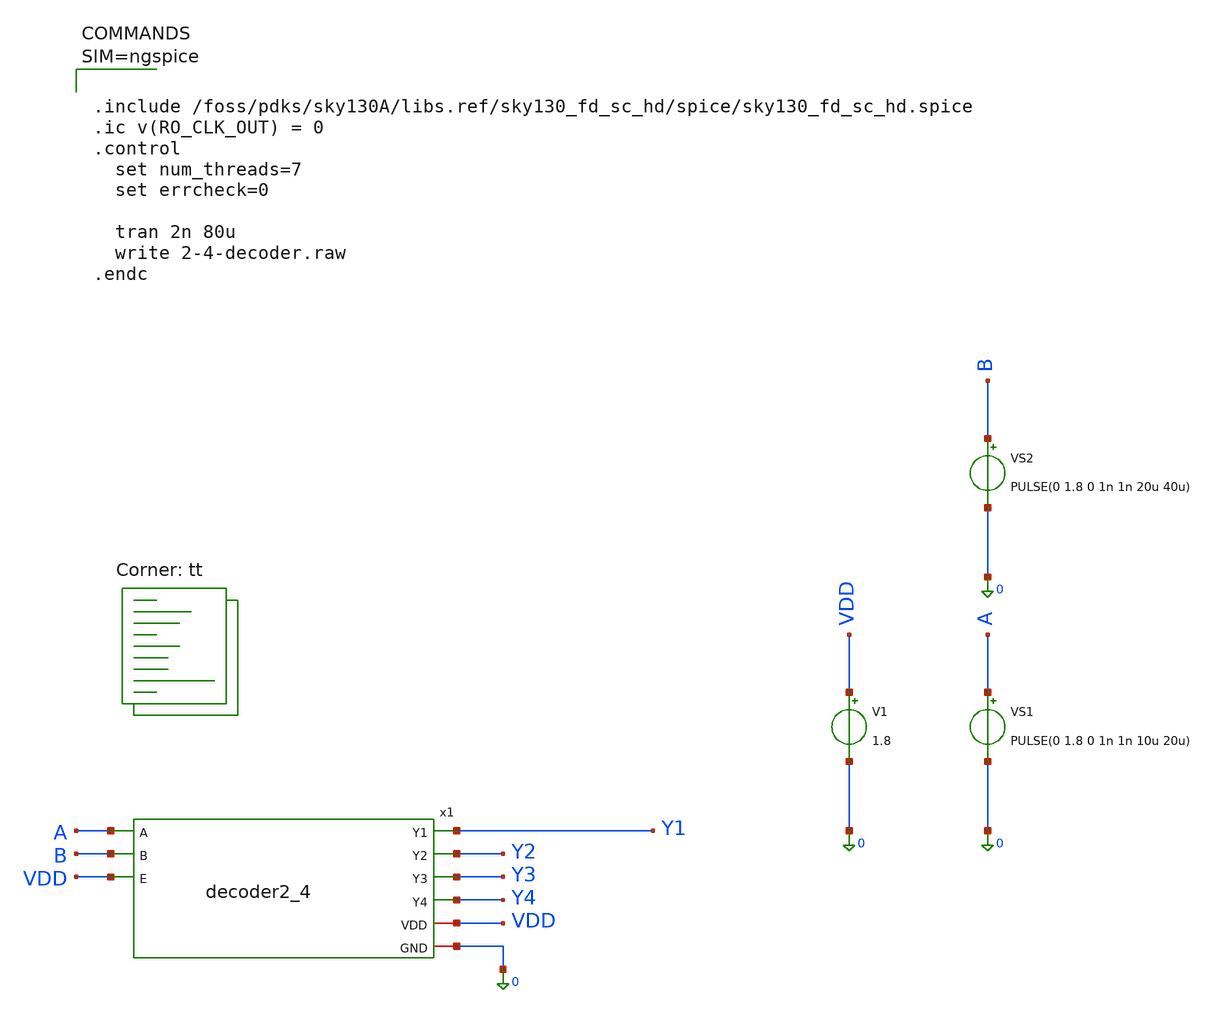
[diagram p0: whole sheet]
** sch_path: src/analog_source_files/decoder2_4_tb.sch
**.subckt decoder2_4_tb
V1 VDD 0 1.8
VS1 A 0 PULSE(0 1.8 0 1n 1n 10u 20u)
VS2 B 0 PULSE(0 1.8 0 1n 1n 20u 40u)
x1 A B Y1 Y2 Y3 Y4 VDD VDD 0 decoder2_4
**** begin user architecture code
.lib $::SKYWATER_MODELS/sky130.lib.spice tt



.include /foss/pdks/sky130A/libs.ref/sky130_fd_sc_hd/spice/sky130_fd_sc_hd.spice
.ic v(RO_CLK_OUT) = 0
.control
  set num_threads=7
  set errcheck=0

  tran 2n 80u
  write 2-4-decoder.raw
.endc



**** end user architecture code
**.ends

* expanding   symbol:  decoder2_4.sym # of pins=9
** sym_path: src/analog_source_files/decoder2_4.sym
** sch_path: src/analog_source_files/decoder2_4.sch
.subckt decoder2_4 A B Y1 Y2 Y3 Y4 E VDD GND
*.ipin E
*.ipin B
*.ipin A
*.opin Y1
*.opin Y2
*.opin Y3
*.opin Y4
*.iopin VDD
*.iopin GND
x1 net1 net2 E GND GND VDD VDD Y1 sky130_fd_sc_hd__and3_2
x2 A net2 E GND GND VDD VDD Y2 sky130_fd_sc_hd__and3_2
x3 net1 B E GND GND VDD VDD Y3 sky130_fd_sc_hd__and3_2
x4 A B E GND GND VDD VDD Y4 sky130_fd_sc_hd__and3_2
x5 A GND GND VDD VDD net1 sky130_fd_sc_hd__inv_1
x6 B GND GND VDD VDD net2 sky130_fd_sc_hd__inv_1
.ends

.end
